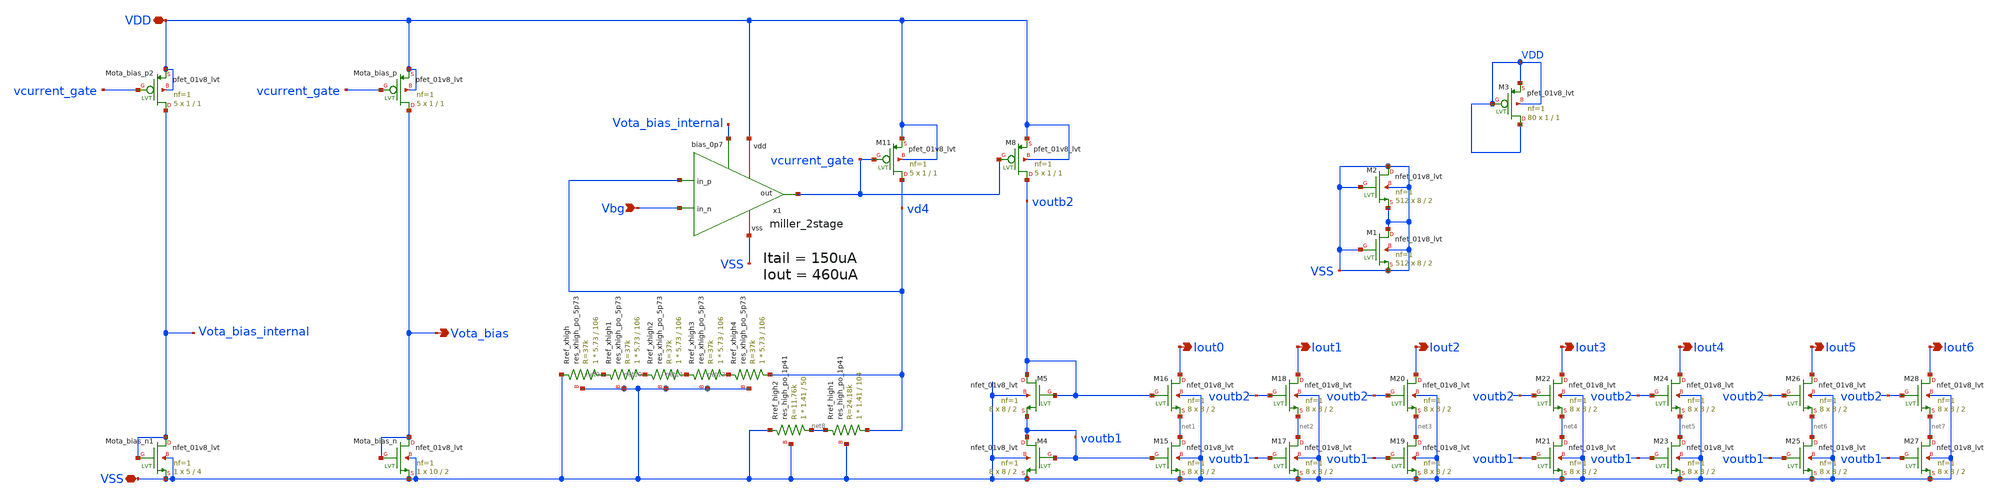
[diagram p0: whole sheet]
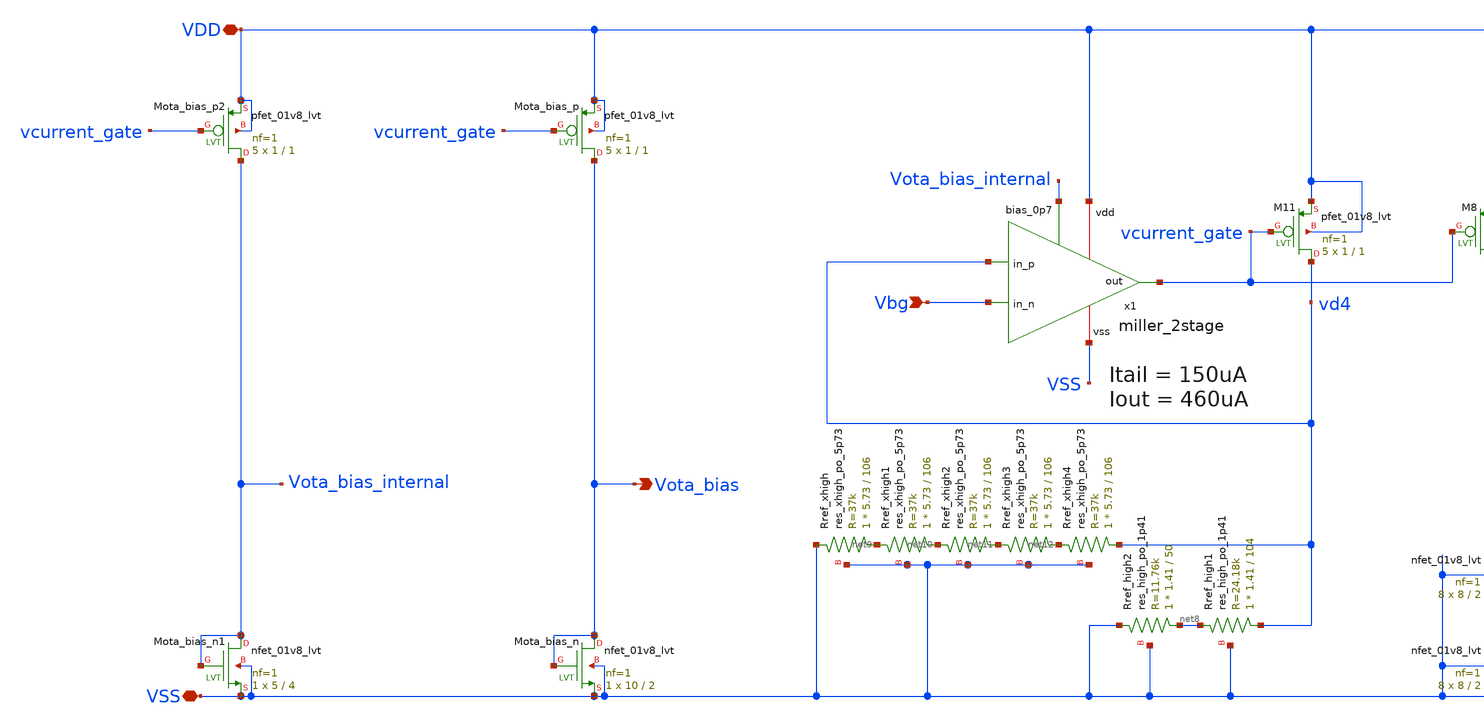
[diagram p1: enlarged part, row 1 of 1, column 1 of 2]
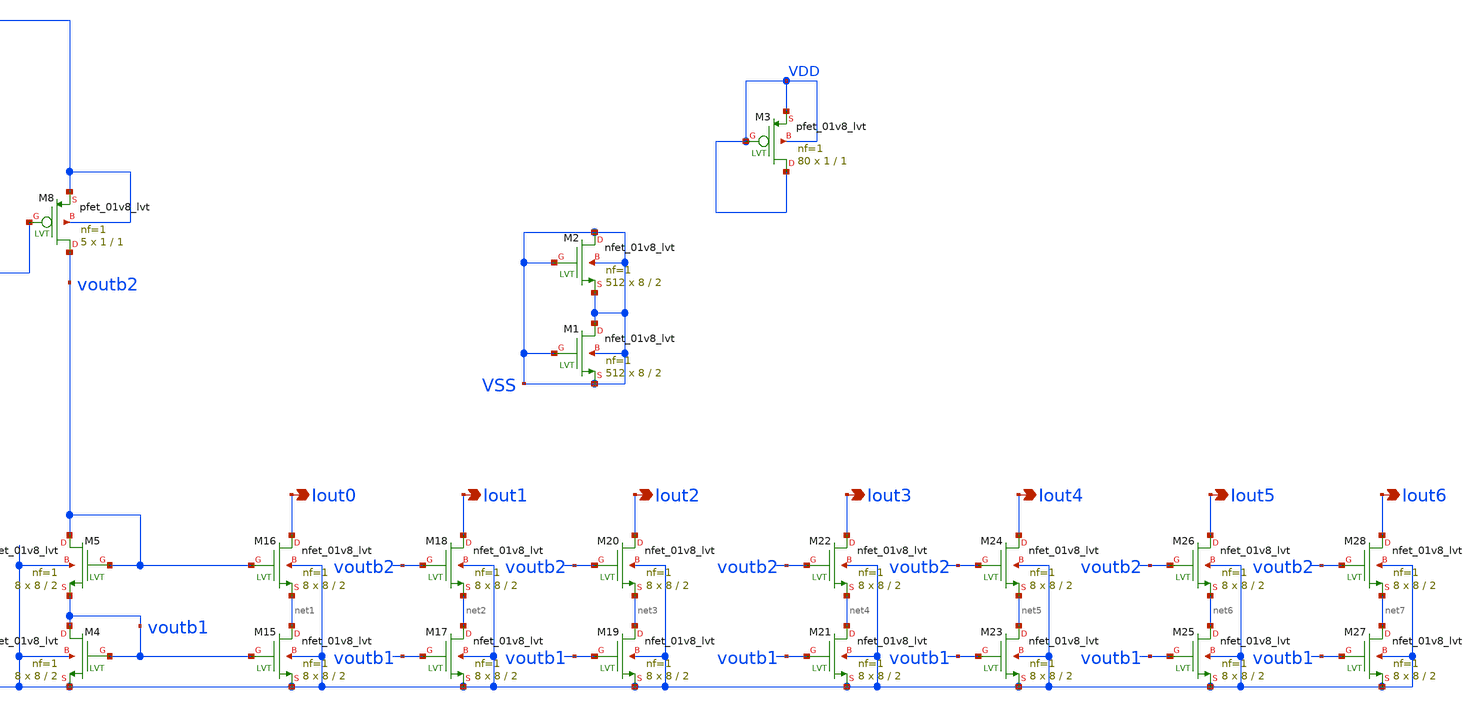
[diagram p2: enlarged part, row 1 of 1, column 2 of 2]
** sch_path: xschem/current_reference/current_ref.sch
**.subckt current_ref Iout0 Iout1 Iout2 Iout3 Iout4 Iout5 Iout6 Vbg Vota_bias VDD VSS
*.opin Iout0
*.opin Iout1
*.opin Iout2
*.opin Iout3
*.opin Iout4
*.opin Iout5
*.opin Iout6
*.ipin Vbg
*.opin Vota_bias
*.iopin VDD
*.iopin VSS
XMota_bias_n Vota_bias Vota_bias VSS VSS sky130_fd_pr__nfet_01v8_lvt L=2 W=10 nf=1 ad='int((nf+1)/2) * W/nf * 0.29'
+ as='int((nf+2)/2) * W/nf * 0.29' pd='2*int((nf+1)/2) * (W/nf + 0.29)' ps='2*int((nf+2)/2) * (W/nf + 0.29)'
+ nrd='0.29 / W' nrs='0.29 / W' sa=0 sb=0 sd=0 mult=1 m=1
XMota_bias_p Vota_bias vcurrent_gate VDD VDD sky130_fd_pr__pfet_01v8_lvt L=1 W=1 nf=1 ad='int((nf+1)/2) * W/nf * 0.29'
+ as='int((nf+2)/2) * W/nf * 0.29' pd='2*int((nf+1)/2) * (W/nf + 0.29)' ps='2*int((nf+2)/2) * (W/nf + 0.29)'
+ nrd='0.29 / W' nrs='0.29 / W' sa=0 sb=0 sd=0 mult=5 m=5
XM11 vd4 vcurrent_gate VDD VDD sky130_fd_pr__pfet_01v8_lvt L=1 W=1 nf=1 ad='int((nf+1)/2) * W/nf * 0.29'
+ as='int((nf+2)/2) * W/nf * 0.29' pd='2*int((nf+1)/2) * (W/nf + 0.29)' ps='2*int((nf+2)/2) * (W/nf + 0.29)'
+ nrd='0.29 / W' nrs='0.29 / W' sa=0 sb=0 sd=0 mult=5 m=5
XM8 voutb2 vcurrent_gate VDD VDD sky130_fd_pr__pfet_01v8_lvt L=1 W=1 nf=1 ad='int((nf+1)/2) * W/nf * 0.29'
+ as='int((nf+2)/2) * W/nf * 0.29' pd='2*int((nf+1)/2) * (W/nf + 0.29)' ps='2*int((nf+2)/2) * (W/nf + 0.29)'
+ nrd='0.29 / W' nrs='0.29 / W' sa=0 sb=0 sd=0 mult=5 m=5
XM4 voutb1 voutb1 VSS VSS sky130_fd_pr__nfet_01v8_lvt L=2 W=8 nf=1 ad='int((nf+1)/2) * W/nf * 0.29' as='int((nf+2)/2) * W/nf * 0.29'
+ pd='2*int((nf+1)/2) * (W/nf + 0.29)' ps='2*int((nf+2)/2) * (W/nf + 0.29)' nrd='0.29 / W' nrs='0.29 / W'
+ sa=0 sb=0 sd=0 mult=8 m=8
XM5 voutb2 voutb2 voutb1 VSS sky130_fd_pr__nfet_01v8_lvt L=2 W=8 nf=1 ad='int((nf+1)/2) * W/nf * 0.29'
+ as='int((nf+2)/2) * W/nf * 0.29' pd='2*int((nf+1)/2) * (W/nf + 0.29)' ps='2*int((nf+2)/2) * (W/nf + 0.29)'
+ nrd='0.29 / W' nrs='0.29 / W' sa=0 sb=0 sd=0 mult=8 m=8
XM15 net1 voutb1 VSS VSS sky130_fd_pr__nfet_01v8_lvt L=2 W=8 nf=1 ad='int((nf+1)/2) * W/nf * 0.29' as='int((nf+2)/2) * W/nf * 0.29'
+ pd='2*int((nf+1)/2) * (W/nf + 0.29)' ps='2*int((nf+2)/2) * (W/nf + 0.29)' nrd='0.29 / W' nrs='0.29 / W'
+ sa=0 sb=0 sd=0 mult=8 m=8
XM16 Iout0 voutb2 net1 VSS sky130_fd_pr__nfet_01v8_lvt L=2 W=8 nf=1 ad='int((nf+1)/2) * W/nf * 0.29'
+ as='int((nf+2)/2) * W/nf * 0.29' pd='2*int((nf+1)/2) * (W/nf + 0.29)' ps='2*int((nf+2)/2) * (W/nf + 0.29)'
+ nrd='0.29 / W' nrs='0.29 / W' sa=0 sb=0 sd=0 mult=8 m=8
XM17 net2 voutb1 VSS VSS sky130_fd_pr__nfet_01v8_lvt L=2 W=8 nf=1 ad='int((nf+1)/2) * W/nf * 0.29' as='int((nf+2)/2) * W/nf * 0.29'
+ pd='2*int((nf+1)/2) * (W/nf + 0.29)' ps='2*int((nf+2)/2) * (W/nf + 0.29)' nrd='0.29 / W' nrs='0.29 / W'
+ sa=0 sb=0 sd=0 mult=8 m=8
XM18 Iout1 voutb2 net2 VSS sky130_fd_pr__nfet_01v8_lvt L=2 W=8 nf=1 ad='int((nf+1)/2) * W/nf * 0.29'
+ as='int((nf+2)/2) * W/nf * 0.29' pd='2*int((nf+1)/2) * (W/nf + 0.29)' ps='2*int((nf+2)/2) * (W/nf + 0.29)'
+ nrd='0.29 / W' nrs='0.29 / W' sa=0 sb=0 sd=0 mult=8 m=8
XM19 net3 voutb1 VSS VSS sky130_fd_pr__nfet_01v8_lvt L=2 W=8 nf=1 ad='int((nf+1)/2) * W/nf * 0.29' as='int((nf+2)/2) * W/nf * 0.29'
+ pd='2*int((nf+1)/2) * (W/nf + 0.29)' ps='2*int((nf+2)/2) * (W/nf + 0.29)' nrd='0.29 / W' nrs='0.29 / W'
+ sa=0 sb=0 sd=0 mult=8 m=8
XM20 Iout2 voutb2 net3 VSS sky130_fd_pr__nfet_01v8_lvt L=2 W=8 nf=1 ad='int((nf+1)/2) * W/nf * 0.29'
+ as='int((nf+2)/2) * W/nf * 0.29' pd='2*int((nf+1)/2) * (W/nf + 0.29)' ps='2*int((nf+2)/2) * (W/nf + 0.29)'
+ nrd='0.29 / W' nrs='0.29 / W' sa=0 sb=0 sd=0 mult=8 m=8
XM21 net4 voutb1 VSS VSS sky130_fd_pr__nfet_01v8_lvt L=2 W=8 nf=1 ad='int((nf+1)/2) * W/nf * 0.29' as='int((nf+2)/2) * W/nf * 0.29'
+ pd='2*int((nf+1)/2) * (W/nf + 0.29)' ps='2*int((nf+2)/2) * (W/nf + 0.29)' nrd='0.29 / W' nrs='0.29 / W'
+ sa=0 sb=0 sd=0 mult=8 m=8
XM22 Iout3 voutb2 net4 VSS sky130_fd_pr__nfet_01v8_lvt L=2 W=8 nf=1 ad='int((nf+1)/2) * W/nf * 0.29'
+ as='int((nf+2)/2) * W/nf * 0.29' pd='2*int((nf+1)/2) * (W/nf + 0.29)' ps='2*int((nf+2)/2) * (W/nf + 0.29)'
+ nrd='0.29 / W' nrs='0.29 / W' sa=0 sb=0 sd=0 mult=8 m=8
XM23 net5 voutb1 VSS VSS sky130_fd_pr__nfet_01v8_lvt L=2 W=8 nf=1 ad='int((nf+1)/2) * W/nf * 0.29' as='int((nf+2)/2) * W/nf * 0.29'
+ pd='2*int((nf+1)/2) * (W/nf + 0.29)' ps='2*int((nf+2)/2) * (W/nf + 0.29)' nrd='0.29 / W' nrs='0.29 / W'
+ sa=0 sb=0 sd=0 mult=8 m=8
XM24 Iout4 voutb2 net5 VSS sky130_fd_pr__nfet_01v8_lvt L=2 W=8 nf=1 ad='int((nf+1)/2) * W/nf * 0.29'
+ as='int((nf+2)/2) * W/nf * 0.29' pd='2*int((nf+1)/2) * (W/nf + 0.29)' ps='2*int((nf+2)/2) * (W/nf + 0.29)'
+ nrd='0.29 / W' nrs='0.29 / W' sa=0 sb=0 sd=0 mult=8 m=8
XM25 net6 voutb1 VSS VSS sky130_fd_pr__nfet_01v8_lvt L=2 W=8 nf=1 ad='int((nf+1)/2) * W/nf * 0.29' as='int((nf+2)/2) * W/nf * 0.29'
+ pd='2*int((nf+1)/2) * (W/nf + 0.29)' ps='2*int((nf+2)/2) * (W/nf + 0.29)' nrd='0.29 / W' nrs='0.29 / W'
+ sa=0 sb=0 sd=0 mult=8 m=8
XM26 Iout5 voutb2 net6 VSS sky130_fd_pr__nfet_01v8_lvt L=2 W=8 nf=1 ad='int((nf+1)/2) * W/nf * 0.29'
+ as='int((nf+2)/2) * W/nf * 0.29' pd='2*int((nf+1)/2) * (W/nf + 0.29)' ps='2*int((nf+2)/2) * (W/nf + 0.29)'
+ nrd='0.29 / W' nrs='0.29 / W' sa=0 sb=0 sd=0 mult=8 m=8
XM27 net7 voutb1 VSS VSS sky130_fd_pr__nfet_01v8_lvt L=2 W=8 nf=1 ad='int((nf+1)/2) * W/nf * 0.29' as='int((nf+2)/2) * W/nf * 0.29'
+ pd='2*int((nf+1)/2) * (W/nf + 0.29)' ps='2*int((nf+2)/2) * (W/nf + 0.29)' nrd='0.29 / W' nrs='0.29 / W'
+ sa=0 sb=0 sd=0 mult=8 m=8
XM28 Iout6 voutb2 net7 VSS sky130_fd_pr__nfet_01v8_lvt L=2 W=8 nf=1 ad='int((nf+1)/2) * W/nf * 0.29'
+ as='int((nf+2)/2) * W/nf * 0.29' pd='2*int((nf+1)/2) * (W/nf + 0.29)' ps='2*int((nf+2)/2) * (W/nf + 0.29)'
+ nrd='0.29 / W' nrs='0.29 / W' sa=0 sb=0 sd=0 mult=8 m=8
XRref_xhigh net9 VSS VSS sky130_fd_pr__res_xhigh_po_5p73 L=106 mult=1 m=1
XRref_xhigh1 net10 net9 VSS sky130_fd_pr__res_xhigh_po_5p73 L=106 mult=1 m=1
XRref_xhigh2 net11 net10 VSS sky130_fd_pr__res_xhigh_po_5p73 L=106 mult=1 m=1
XRref_xhigh3 net12 net11 VSS sky130_fd_pr__res_xhigh_po_5p73 L=106 mult=1 m=1
XRref_xhigh4 vd4 net12 VSS sky130_fd_pr__res_xhigh_po_5p73 L=106 mult=1 m=1
XRref_high1 vd4 net8 VSS sky130_fd_pr__res_high_po_1p41 L=104 mult=1 m=1
XRref_high2 net8 VSS VSS sky130_fd_pr__res_high_po_1p41 L=50 mult=1 m=1
XM1 VSS VSS VSS VSS sky130_fd_pr__nfet_01v8_lvt L=2 W=8 nf=1 ad='int((nf+1)/2) * W/nf * 0.29' as='int((nf+2)/2) * W/nf * 0.29'
+ pd='2*int((nf+1)/2) * (W/nf + 0.29)' ps='2*int((nf+2)/2) * (W/nf + 0.29)' nrd='0.29 / W' nrs='0.29 / W'
+ sa=0 sb=0 sd=0 mult=512 m=512
XM2 VSS VSS VSS VSS sky130_fd_pr__nfet_01v8_lvt L=2 W=8 nf=1 ad='int((nf+1)/2) * W/nf * 0.29' as='int((nf+2)/2) * W/nf * 0.29'
+ pd='2*int((nf+1)/2) * (W/nf + 0.29)' ps='2*int((nf+2)/2) * (W/nf + 0.29)' nrd='0.29 / W' nrs='0.29 / W'
+ sa=0 sb=0 sd=0 mult=512 m=512
XM3 VDD VDD VDD VDD sky130_fd_pr__pfet_01v8_lvt L=1 W=1 nf=1 ad='int((nf+1)/2) * W/nf * 0.29' as='int((nf+2)/2) * W/nf * 0.29'
+ pd='2*int((nf+1)/2) * (W/nf + 0.29)' ps='2*int((nf+2)/2) * (W/nf + 0.29)' nrd='0.29 / W' nrs='0.29 / W'
+ sa=0 sb=0 sd=0 mult=80 m=80
x1 VDD Vbg vd4 vcurrent_gate Vota_bias_internal VSS miller_2stage
XMota_bias_n1 Vota_bias_internal Vota_bias_internal VSS VSS sky130_fd_pr__nfet_01v8_lvt L=4 W=5 nf=1
+ ad='int((nf+1)/2) * W/nf * 0.29' as='int((nf+2)/2) * W/nf * 0.29' pd='2*int((nf+1)/2) * (W/nf + 0.29)'
+ ps='2*int((nf+2)/2) * (W/nf + 0.29)' nrd='0.29 / W' nrs='0.29 / W' sa=0 sb=0 sd=0 mult=1 m=1
XMota_bias_p2 Vota_bias_internal vcurrent_gate VDD VDD sky130_fd_pr__pfet_01v8_lvt L=1 W=1 nf=1 ad='int((nf+1)/2) * W/nf * 0.29'
+ as='int((nf+2)/2) * W/nf * 0.29' pd='2*int((nf+1)/2) * (W/nf + 0.29)' ps='2*int((nf+2)/2) * (W/nf + 0.29)'
+ nrd='0.29 / W' nrs='0.29 / W' sa=0 sb=0 sd=0 mult=5 m=5
**.ends
.end
